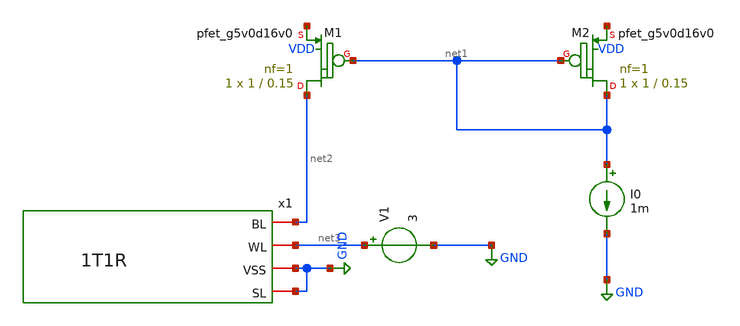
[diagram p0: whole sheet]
** sch_path: xschem/untitled-3.sch
* StefanSchippers/xschem_sky130/sky130_fd_pr/reram.sym:
* Copyright 2021 Stefan Frederik Schippers
* Licensed under the Apache License, Version 2.0 (the "License");
**.subckt untitled-3
x1 net2 net3 GND GND 1T1R
XM1 net2 net1 net4 VDD sky130_fd_pr__pfet_g5v0d16v0 L=0.15 W=1 nf=1 ad='int((nf+1)/2) * W/nf * 0.29'
+ as='int((nf+2)/2) * W/nf * 0.29' pd='2*int((nf+1)/2) * (W/nf + 0.29)' ps='2*int((nf+2)/2) * (W/nf + 0.29)'
+ nrd='0.29 / W' nrs='0.29 / W' sa=0 sb=0 sd=0 mult=1 m=1
XM2 net1 net1 net5 VDD sky130_fd_pr__pfet_g5v0d16v0 L=0.15 W=1 nf=1 ad='int((nf+1)/2) * W/nf * 0.29'
+ as='int((nf+2)/2) * W/nf * 0.29' pd='2*int((nf+1)/2) * (W/nf + 0.29)' ps='2*int((nf+2)/2) * (W/nf + 0.29)'
+ nrd='0.29 / W' nrs='0.29 / W' sa=0 sb=0 sd=0 mult=1 m=1
I0 net1 GND 1m
V1 net3 GND 3
**.ends

* expanding   symbol:  1T1R.sym # of pins=4
** sym_path: xschem/1T1R.sym
** sch_path: xschem/1T1R.sch
.subckt 1T1R BL WL VSS SL
*.iopin SL
*.iopin VSS
*.iopin WL
*.iopin BL
XR1 BL net1 sky130_fd_pr_reram__reram_cell Tfilament_0=3.8e-9
XM1 net1 WL SL VSS sky130_fd_pr__nfet_g5v0d10v5 L=0.5 W=7 nf=1 ad='int((nf+1)/2) * W/nf * 0.29' as='int((nf+2)/2) * W/nf * 0.29'
+ pd='2*int((nf+1)/2) * (W/nf + 0.29)' ps='2*int((nf+2)/2) * (W/nf + 0.29)' nrd='0.29 / W' nrs='0.29 / W'
+ sa=0 sb=0 sd=0 mult=1 m=1
.ends

.GLOBAL GND
**** begin user architecture code

.subckt sky130_fd_pr_reram__reram_cell TE BE Tfilament_0=3.3e-9 area_ox=0.1024e-12
N1 TE BE nFilament sky130_fd_pr_reram__reram_model
.ic v(nFilament)={Tfilament_0*1.0e9}
.ends sky130_fd_pr_reram__reram_cell

.model sky130_fd_pr_reram__reram_model sky130_fd_pr_reram__reram_module  area_ox = 0.1024e-12  Tox =
+ 5.0  Tfilament_max = 4.9  Tfilament_min = 3.3  Eact_generation = 1.501  Eact_recombination  = 1.500
+  I_k1  = 6.140e-5  Tfilament_ref = 4.7249  V_ref = 0.430  velocity_k1 = 150  gamma_k0  = 16.5  gamma_k1
+  = -1.25  Temperature_0 = 300  C_thermal = 3.1825e-16  tau_thermal = 0.23e-9  t_step  = 1.0e-9
+  smoothing = 1e-7  Kclip = 200

.control
pre_osdi $SKYWATER_MODELS/sky130_fd_pr_reram__reram_module.osdi
.endc

**** end user architecture code
.end
